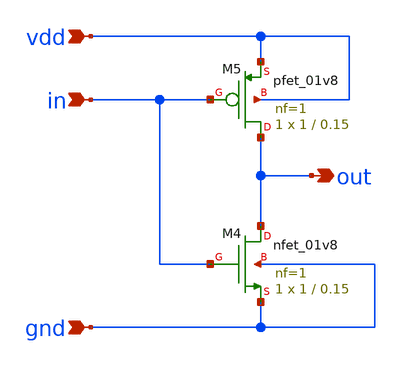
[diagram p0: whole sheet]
** sch_path: inverter/inverterr.sch
**.subckt inverterr vdd in gnd out
*.ipin vdd
*.ipin in
*.ipin gnd
*.opin out
XM4 out in gnd gnd sky130_fd_pr__nfet_01v8 L=0.15 W=1 nf=1 ad='int((nf+1)/2) * W/nf * 0.29' as='int((nf+2)/2) * W/nf * 0.29'
+ pd='2*int((nf+1)/2) * (W/nf + 0.29)' ps='2*int((nf+2)/2) * (W/nf + 0.29)' nrd='0.29 / W' nrs='0.29 / W'
+ sa=0 sb=0 sd=0 mult=1 m=1
XM5 out in vdd vdd sky130_fd_pr__pfet_01v8 L=0.15 W=1 nf=1 ad='int((nf+1)/2) * W/nf * 0.29' as='int((nf+2)/2) * W/nf * 0.29'
+ pd='2*int((nf+1)/2) * (W/nf + 0.29)' ps='2*int((nf+2)/2) * (W/nf + 0.29)' nrd='0.29 / W' nrs='0.29 / W'
+ sa=0 sb=0 sd=0 mult=1 m=1
**.ends
.end
